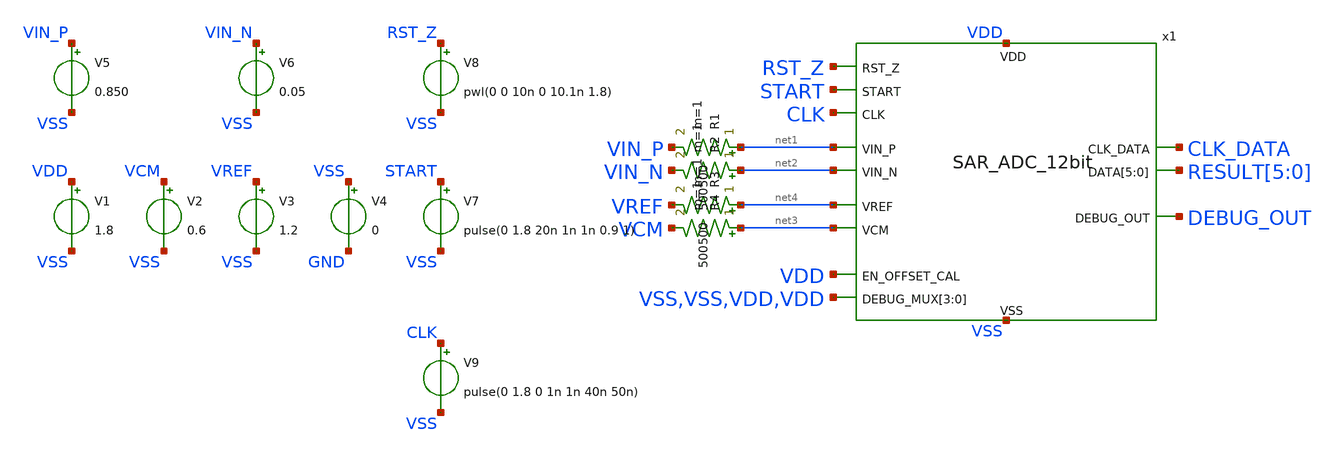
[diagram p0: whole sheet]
** sch_path: sim/SAR_ADC_12bit_sim.sch

.lib $::SKYWATER_MODELS/sky130.lib.spice tt
.include /opt/pdk/share/pdk/sky130A/libs.tech/combined/continuous/models_diodes.spice
.include /opt/pdk/share/pdk/sky130A/libs.tech/ngspice/sky130_fd_pr__model__r+c.model.spice
.include $::SKYWATER_STDCELLS/sky130_fd_sc_hd.spice
.include ~/Desktop/SAR_ADC_12b/SAR_ADC_12bit/CDAC/New_CDAC/CDAC_12bit.spice
.include ~/Desktop/SAR_ADC_12b/SAR_ADC_12bit/state_machine/layout/state_machine_single_ended.spice
*.include ~/Desktop/SAR_ADC_12b/SAR_ADC_12bit/layout/SAR_ADC_12bit_flat.spice

**.subckt SAR_ADC_12bit_sim
V1 VDD VSS 1.8
.save i(v1)
V2 VCM VSS 0.6
.save i(v2)
V3 VREF VSS 1.2
.save i(v3)
V4 VSS GND 0
V6 VIN_N VSS 0.05
V7 START VSS pulse(0 1.8 20n 1n 1n 0.9 1)
V8 RST_Z VSS pwl(0 0 10n 0 10.1n 1.8)
V5 VIN_P VSS 0.850
x1 VDD net3 VSS net4 net1 net2 RST_Z CLK_DATA RESULT[5] RESULT[4] RESULT[3] RESULT[2] RESULT[1]
+ RESULT[0] START VDD VSS VSS VDD VDD DEBUG_OUT CLK SAR_ADC_12bit
R1 net1 VIN_P 500 m=1
R2 net2 VIN_N 500 m=1
R3 net4 VREF 500 m=1
R4 net3 VCM 500 m=1
V9 CLK VSS pulse(0 1.8 0 1n 1n 40n 50n)
**** begin user architecture code


.save all
*.save start rst_z vin_p vin_n vref vcm x1.vdac_p x1.vdac_n x1.vdac_pi x1.vdac_ni x1.smpl x1.en_comp x1.comp_p x1.comp_n x1.cal_p x1.cal_n
*.save result[5] result[4] result[3] result[2] result[1] result[0] clk_data debug_out
*.save x1.C10_p_btm x1.C10_n_btm x1.C9_p_btm x1.C9_n_btm x1.C8_p_btm x1.C8_n_btm x1.C7_p_btm x1.C7_n_btm x1.C6_p_btm x1.C6_n_btm x1.C5_p_btm x1.C5_n_btm x1.C4_p_btm x1.C4_n_btm x1.C3_p_btm x1.C3_n_btm x1.C2_p_btm x1.C2_n_btm x1.C1_p_btm x1.C1_n_btm x1.C0_p_btm x1.C0_n_btm x1.C0_dummy_p_btm x1.C0_dummy_n_btm
*.save x1.en_vin_bstr_p x1.en_vin_bstr_n
*.option method = gear
.option GMIN=1e-12 reltol=1e-5
.control
		set num_threads=8
		tran 10n 0.9u
		write SAR_ADC_12bit_sim.raw
.endc


**** end user architecture code
**.ends
.end
